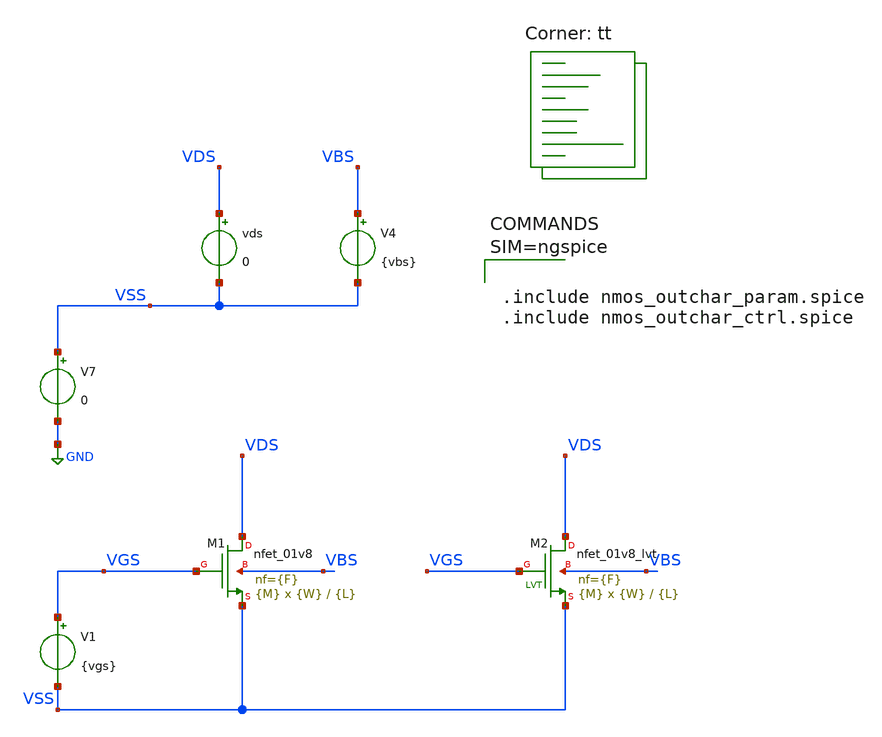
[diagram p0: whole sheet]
** sch_path: work/design/nmos_outchar.sch
**.subckt nmos_outchar
XM1 VDS VGS VSS VBS sky130_fd_pr__nfet_01v8 L={L} W={W} nf={F} ad='int((nf+1)/2) * W/nf * 0.29' as='int((nf+2)/2) * W/nf * 0.29'
+ pd='2*int((nf+1)/2) * (W/nf + 0.29)' ps='2*int((nf+2)/2) * (W/nf + 0.29)' nrd='0.29 / W' nrs='0.29 / W'
+ sa=0 sb=0 sd=0 mult={M} m={M}
V1 VGS VSS {vgs}
V4 VBS VSS {vbs}
V7 VSS GND 0
vds VDS VSS 0
XM2 VDS VGS VSS VBS sky130_fd_pr__nfet_01v8_lvt L={L} W={W} nf={F} ad='int((nf+1)/2) * W/nf * 0.29' as='int((nf+2)/2) * W/nf * 0.29'
+ pd='2*int((nf+1)/2) * (W/nf + 0.29)' ps='2*int((nf+2)/2) * (W/nf + 0.29)' nrd='0.29 / W' nrs='0.29 / W'
+ sa=0 sb=0 sd=0 mult={M} m={M}
**** begin user architecture code
.lib $::SKYWATER_MODELS/sky130.lib.spice tt



.include nmos_outchar_param.spice
.include nmos_outchar_ctrl.spice



**** end user architecture code
**.ends
.GLOBAL GND
.end
